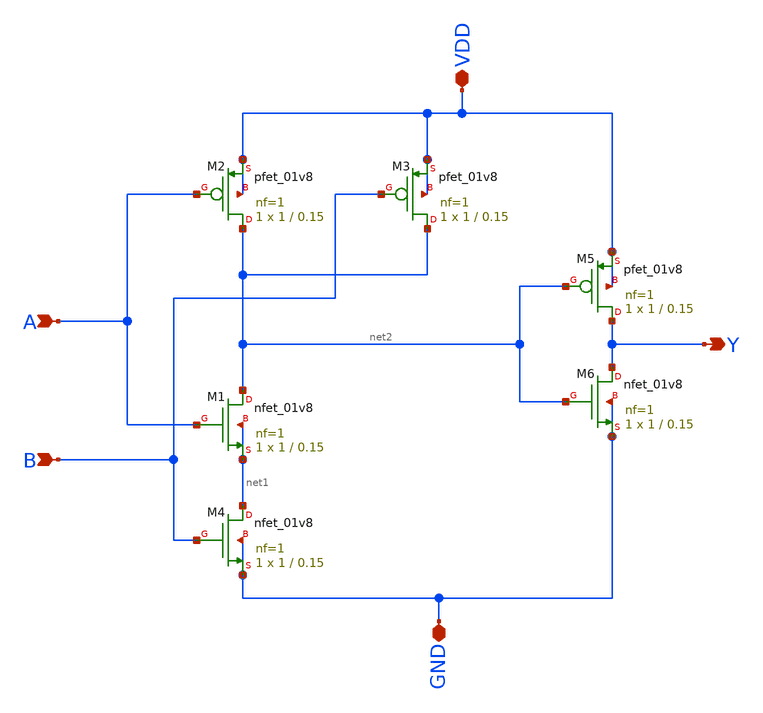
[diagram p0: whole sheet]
** sch_path: designs/and/xschem/and.sch
**.subckt and B A Y VDD GND
*.ipin B
*.ipin A
*.opin Y
*.iopin VDD
*.iopin GND
XM1 net2 A net1 net1 sky130_fd_pr__nfet_01v8 L=0.15 W=1 nf=1 ad='int((1 + 1)/2) * 1 / 1 * 0.29' as='int((1 + 2)/2) * 1 / 1 * 0.29'
+ pd='2*int((1 + 1)/2) * (1 / 1 + 0.29)' ps='2*int((1 + 2)/2) * (1 / 1 + 0.29)' nrd='0.29 / 1 ' nrs='0.29 / 1 '
+ sa=0 sb=0 sd=0 mult=1 m=1
XM2 net2 A VDD VDD sky130_fd_pr__pfet_01v8 L=0.15 W=1 nf=1 ad='int((1 + 1)/2) * 1 / 1 * 0.29' as='int((1 + 2)/2) * 1 / 1 * 0.29'
+ pd='2*int((1 + 1)/2) * (1 / 1 + 0.29)' ps='2*int((1 + 2)/2) * (1 / 1 + 0.29)' nrd='0.29 / 1 ' nrs='0.29 / 1 '
+ sa=0 sb=0 sd=0 mult=1 m=1
XM3 net2 B VDD VDD sky130_fd_pr__pfet_01v8 L=0.15 W=1 nf=1 ad='int((1 + 1)/2) * 1 / 1 * 0.29' as='int((1 + 2)/2) * 1 / 1 * 0.29'
+ pd='2*int((1 + 1)/2) * (1 / 1 + 0.29)' ps='2*int((1 + 2)/2) * (1 / 1 + 0.29)' nrd='0.29 / 1 ' nrs='0.29 / 1 '
+ sa=0 sb=0 sd=0 mult=1 m=1
XM4 net1 B GND GND sky130_fd_pr__nfet_01v8 L=0.15 W=1 nf=1 ad='int((1 + 1)/2) * 1 / 1 * 0.29' as='int((1 + 2)/2) * 1 / 1 * 0.29'
+ pd='2*int((1 + 1)/2) * (1 / 1 + 0.29)' ps='2*int((1 + 2)/2) * (1 / 1 + 0.29)' nrd='0.29 / 1 ' nrs='0.29 / 1 '
+ sa=0 sb=0 sd=0 mult=1 m=1
XM5 Y net2 VDD VDD sky130_fd_pr__pfet_01v8 L=0.15 W=1 nf=1 ad='int((1 + 1)/2) * 1 / 1 * 0.29' as='int((1 + 2)/2) * 1 / 1 * 0.29'
+ pd='2*int((1 + 1)/2) * (1 / 1 + 0.29)' ps='2*int((1 + 2)/2) * (1 / 1 + 0.29)' nrd='0.29 / 1 ' nrs='0.29 / 1 '
+ sa=0 sb=0 sd=0 mult=1 m=1
XM6 Y net2 GND GND sky130_fd_pr__nfet_01v8 L=0.15 W=1 nf=1 ad='int((1 + 1)/2) * 1 / 1 * 0.29' as='int((1 + 2)/2) * 1 / 1 * 0.29'
+ pd='2*int((1 + 1)/2) * (1 / 1 + 0.29)' ps='2*int((1 + 2)/2) * (1 / 1 + 0.29)' nrd='0.29 / 1 ' nrs='0.29 / 1 '
+ sa=0 sb=0 sd=0 mult=1 m=1
**.ends
.end
